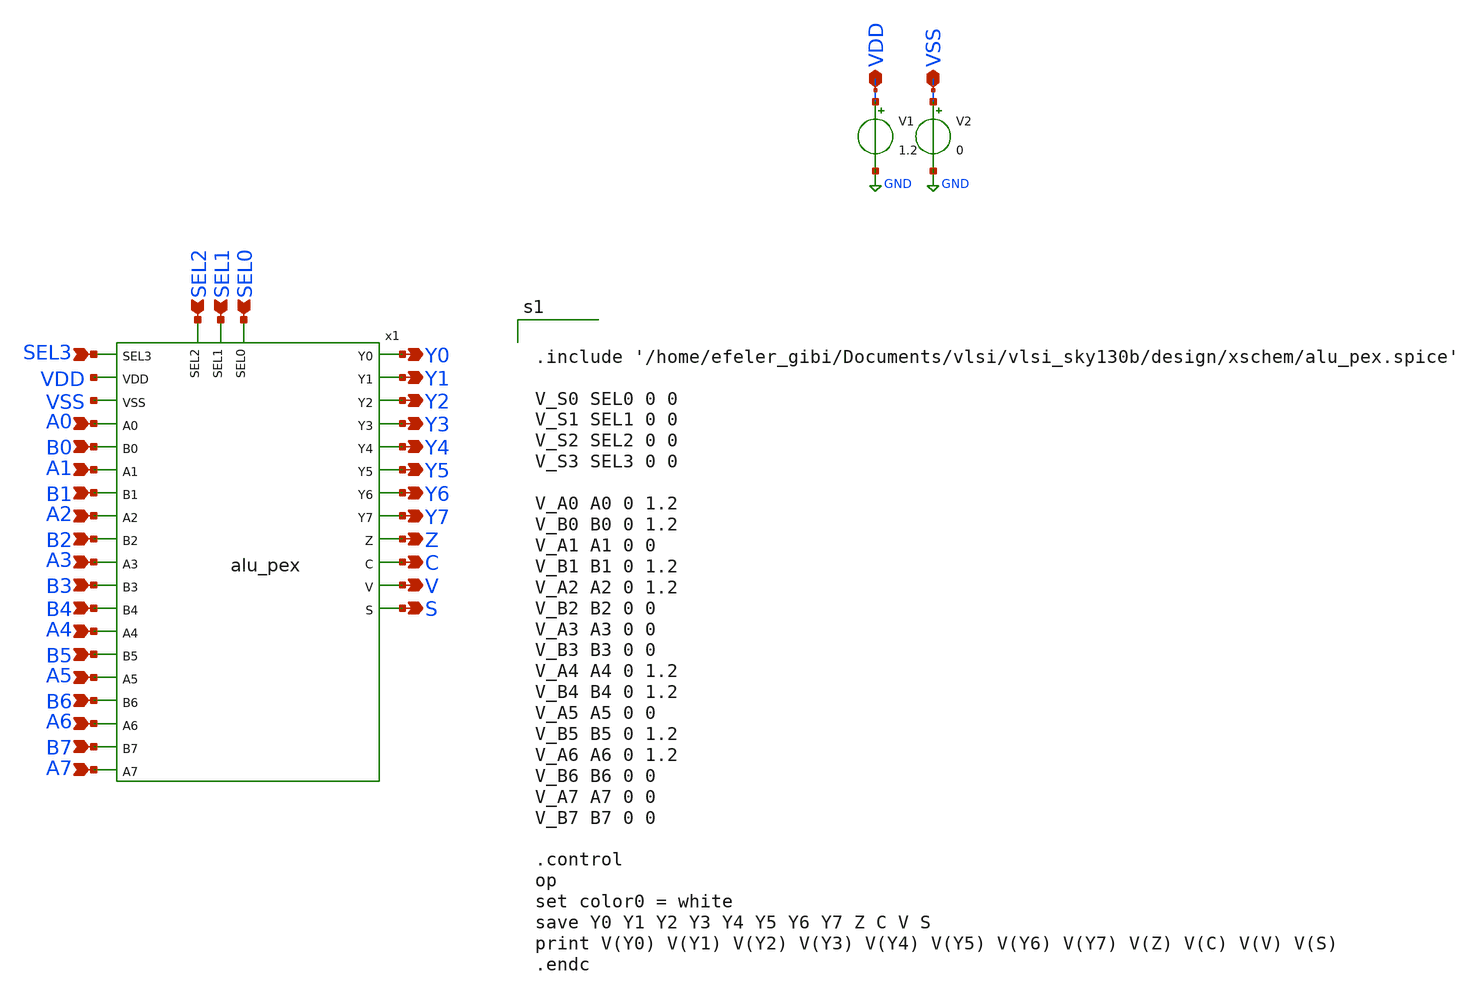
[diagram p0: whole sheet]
** sch_path: design/xschem/TEST_BENCHES/ALUpex_TB_ADD.sch
**.subckt ALUpex_TB_ADD VDD VSS A7 A6 A5 A4 A3 A2 A1 A0 B1 B2 B3 B0 B6 B7 B5 B4 Y0 Y1 Y2 Y3 Y4 Y5 Y6
*+ Y7 Z C V S SEL0 SEL1 SEL2 SEL3
*.iopin VDD
*.iopin VSS
*.ipin A7
*.ipin A6
*.ipin A5
*.ipin A4
*.ipin A3
*.ipin A2
*.ipin A1
*.ipin A0
*.ipin B1
*.ipin B2
*.ipin B3
*.ipin B0
*.ipin B6
*.ipin B7
*.ipin B5
*.ipin B4
*.opin Y0
*.opin Y1
*.opin Y2
*.opin Y3
*.opin Y4
*.opin Y5
*.opin Y6
*.opin Y7
*.opin Z
*.opin C
*.opin V
*.opin S
*.ipin SEL0
*.ipin SEL1
*.ipin SEL2
*.ipin SEL3
V1 VDD GND 1.2
V2 VSS GND 0
x1 SEL3 A0 B0 Y0 Z VDD VSS A1 C B1 Y1 A2 V B2 Y2 S A3 Y3 B3 B4 Y4 A4 B5 A5 Y5 B6 Y6 A6 B7 Y7 A7 SEL2
+ SEL1 SEL0 alu_pex
**** begin user architecture code

** opencircuitdesign pdks install
.lib $::SKYWATER_MODELS/sky130.lib.spice tt_mm




.include '/home/efeler_gibi/Documents/vlsi/vlsi_sky130b/design/xschem/alu_pex.spice'

V_S0 SEL0 0 0
V_S1 SEL1 0 0
V_S2 SEL2 0 0
V_S3 SEL3 0 0

V_A0 A0 0 1.2
V_B0 B0 0 1.2
V_A1 A1 0 0
V_B1 B1 0 1.2
V_A2 A2 0 1.2
V_B2 B2 0 0
V_A3 A3 0 0
V_B3 B3 0 0
V_A4 A4 0 1.2
V_B4 B4 0 1.2
V_A5 A5 0 0
V_B5 B5 0 1.2
V_A6 A6 0 1.2
V_B6 B6 0 0
V_A7 A7 0 0
V_B7 B7 0 0

.control
op
set color0 = white
save Y0 Y1 Y2 Y3 Y4 Y5 Y6 Y7 Z C V S
print V(Y0) V(Y1) V(Y2) V(Y3) V(Y4) V(Y5) V(Y6) V(Y7) V(Z) V(C) V(V) V(S)
.endc



**** end user architecture code
**.ends
.GLOBAL GND
.end
